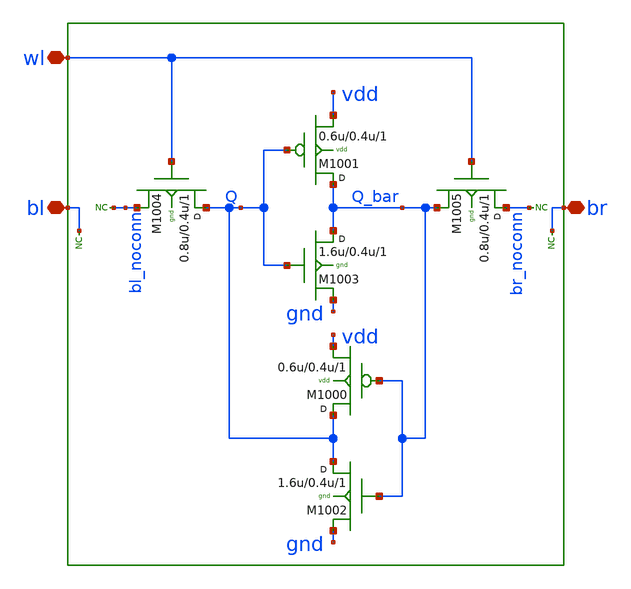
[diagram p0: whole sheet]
** sch_path: sram_2_64_scn4m_lcc/dummy_cell_1rw.sch
**.subckt dummy_cell_1rw bl br wl
*.iopin bl
*.iopin br
*.iopin wl
* noconn bl_noconn
* noconn br_noconn
* noconn br
* noconn bl
M1002 Q Q_bar gnd gnd n w=1.6u l=0.4u m=1
M1004 Q wl bl_noconn gnd n w=0.8u l=0.4u m=1
M1005 br_noconn wl Q_bar gnd n w=0.8u l=0.4u m=1
M1003 Q_bar Q gnd gnd n w=1.6u l=0.4u m=1
M1000 Q Q_bar vdd vdd p w=0.6u l=0.4u m=1
M1001 Q_bar Q vdd vdd p w=0.6u l=0.4u m=1
**.ends
.end
